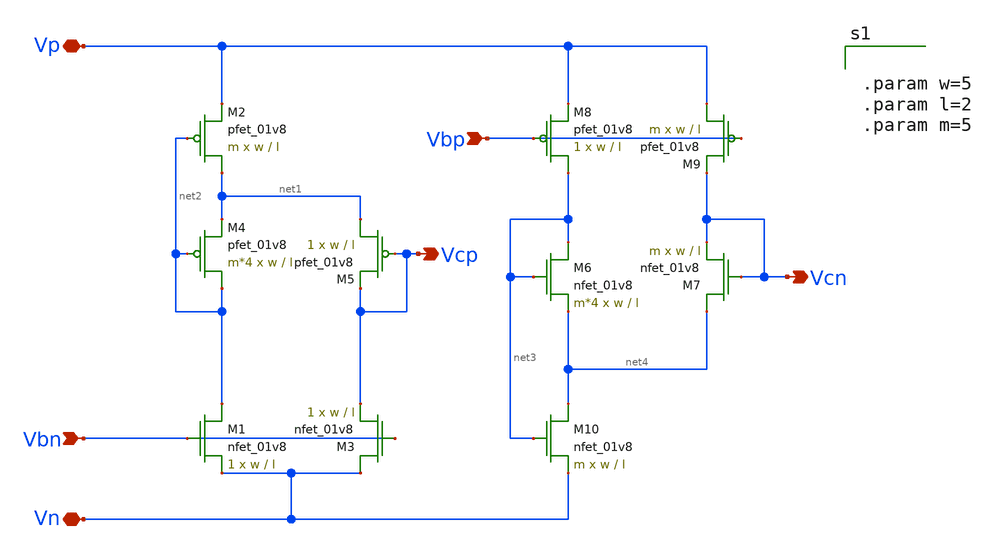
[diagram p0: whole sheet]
** sch_path: schematic/cascode_generator.sch
**.subckt cascode_generator Vbp Vbn Vn Vp Vcp Vcn
*.ipin Vbp
*.ipin Vbn
*.iopin Vn
*.iopin Vp
*.opin Vcp
*.opin Vcn
XM1 net2 Vbn Vn GND sky130_fd_pr__nfet_01v8 L=l W=w nf=1 ad='int((nf+1)/2) * W/nf * 0.29' as='int((nf+2)/2) * W/nf * 0.29'
+ pd='2*int((nf+1)/2) * (W/nf + 0.29)' ps='2*int((nf+2)/2) * (W/nf + 0.29)' nrd='0.29 / W' nrs='0.29 / W'
+ sa=0 sb=0 sd=0 mult=1 m=1
XM2 net1 net2 Vp VDD sky130_fd_pr__pfet_01v8 L=l W=w nf=1 ad='int((nf+1)/2) * W/nf * 0.29' as='int((nf+2)/2) * W/nf * 0.29'
+ pd='2*int((nf+1)/2) * (W/nf + 0.29)' ps='2*int((nf+2)/2) * (W/nf + 0.29)' nrd='0.29 / W' nrs='0.29 / W'
+ sa=0 sb=0 sd=0 mult=m m=m
XM3 Vn Vbn Vcp GND sky130_fd_pr__nfet_01v8 L=l W=w nf=1 ad='int((nf+1)/2) * W/nf * 0.29' as='int((nf+2)/2) * W/nf * 0.29'
+ pd='2*int((nf+1)/2) * (W/nf + 0.29)' ps='2*int((nf+2)/2) * (W/nf + 0.29)' nrd='0.29 / W' nrs='0.29 / W'
+ sa=0 sb=0 sd=0 mult=1 m=1
XM4 net2 net2 net1 VDD sky130_fd_pr__pfet_01v8 L=l W=w nf=1 ad='int((nf+1)/2) * W/nf * 0.29' as='int((nf+2)/2) * W/nf * 0.29'
+ pd='2*int((nf+1)/2) * (W/nf + 0.29)' ps='2*int((nf+2)/2) * (W/nf + 0.29)' nrd='0.29 / W' nrs='0.29 / W'
+ sa=0 sb=0 sd=0 mult=m*4 m=m*4
XM5 net1 Vcp Vcp VDD sky130_fd_pr__pfet_01v8 L=l W=w nf=1 ad='int((nf+1)/2) * W/nf * 0.29' as='int((nf+2)/2) * W/nf * 0.29'
+ pd='2*int((nf+1)/2) * (W/nf + 0.29)' ps='2*int((nf+2)/2) * (W/nf + 0.29)' nrd='0.29 / W' nrs='0.29 / W'
+ sa=0 sb=0 sd=0 mult=1 m=1
XM6 net3 net3 net4 GND sky130_fd_pr__nfet_01v8 L=l W=w nf=1 ad='int((nf+1)/2) * W/nf * 0.29' as='int((nf+2)/2) * W/nf * 0.29'
+ pd='2*int((nf+1)/2) * (W/nf + 0.29)' ps='2*int((nf+2)/2) * (W/nf + 0.29)' nrd='0.29 / W' nrs='0.29 / W'
+ sa=0 sb=0 sd=0 mult=m*4 m=m*4
XM7 net4 Vcn Vcn GND sky130_fd_pr__nfet_01v8 L=l W=w nf=1 ad='int((nf+1)/2) * W/nf * 0.29' as='int((nf+2)/2) * W/nf * 0.29'
+ pd='2*int((nf+1)/2) * (W/nf + 0.29)' ps='2*int((nf+2)/2) * (W/nf + 0.29)' nrd='0.29 / W' nrs='0.29 / W'
+ sa=0 sb=0 sd=0 mult=m m=m
XM8 net3 Vbp Vp VDD sky130_fd_pr__pfet_01v8 L=l W=w nf=1 ad='int((nf+1)/2) * W/nf * 0.29' as='int((nf+2)/2) * W/nf * 0.29'
+ pd='2*int((nf+1)/2) * (W/nf + 0.29)' ps='2*int((nf+2)/2) * (W/nf + 0.29)' nrd='0.29 / W' nrs='0.29 / W'
+ sa=0 sb=0 sd=0 mult=1 m=1
XM9 Vp Vbp Vcn VDD sky130_fd_pr__pfet_01v8 L=l W=w nf=1 ad='int((nf+1)/2) * W/nf * 0.29' as='int((nf+2)/2) * W/nf * 0.29'
+ pd='2*int((nf+1)/2) * (W/nf + 0.29)' ps='2*int((nf+2)/2) * (W/nf + 0.29)' nrd='0.29 / W' nrs='0.29 / W'
+ sa=0 sb=0 sd=0 mult=m m=m
XM10 net4 net3 Vn GND sky130_fd_pr__nfet_01v8 L=l W=w nf=1 ad='int((nf+1)/2) * W/nf * 0.29' as='int((nf+2)/2) * W/nf * 0.29'
+ pd='2*int((nf+1)/2) * (W/nf + 0.29)' ps='2*int((nf+2)/2) * (W/nf + 0.29)' nrd='0.29 / W' nrs='0.29 / W'
+ sa=0 sb=0 sd=0 mult=m m=m
**** begin user architecture code


.param w=5
.param l=2
.param m=5


**** end user architecture code
**.ends
.end
